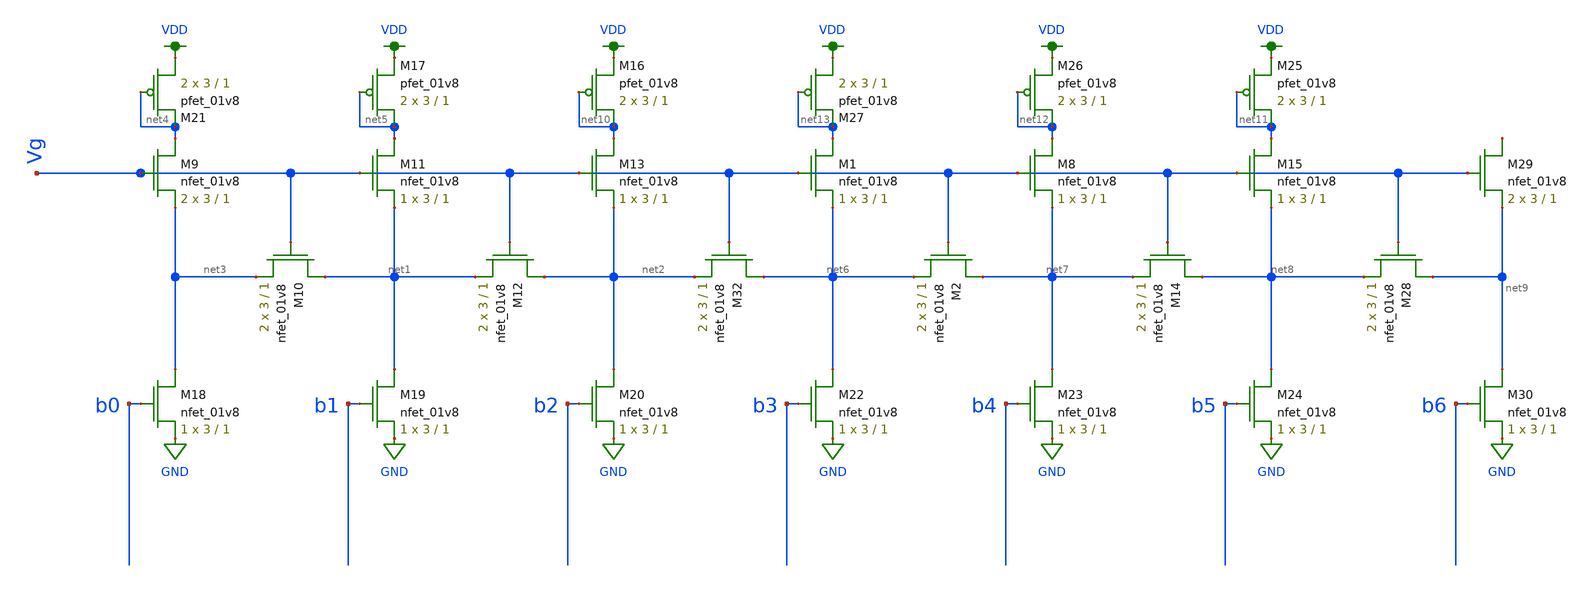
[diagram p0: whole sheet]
** sch_path: schematic/LDS/dac_7_bit.sch
**.subckt dac_7_bit
XM9 net4 Vg net3 GND sky130_fd_pr__nfet_01v8 L=1 W=3 nf=1 ad='int((nf+1)/2) * W/nf * 0.29' as='int((nf+2)/2) * W/nf * 0.29'
+ pd='2*int((nf+1)/2) * (W/nf + 0.29)' ps='2*int((nf+2)/2) * (W/nf + 0.29)' nrd='0.29 / W' nrs='0.29 / W'
+ sa=0 sb=0 sd=0 mult=2 m=2
XM10 net1 Vg net3 GND sky130_fd_pr__nfet_01v8 L=1 W=3 nf=1 ad='int((nf+1)/2) * W/nf * 0.29' as='int((nf+2)/2) * W/nf * 0.29'
+ pd='2*int((nf+1)/2) * (W/nf + 0.29)' ps='2*int((nf+2)/2) * (W/nf + 0.29)' nrd='0.29 / W' nrs='0.29 / W'
+ sa=0 sb=0 sd=0 mult=2 m=2
XM11 net5 Vg net1 GND sky130_fd_pr__nfet_01v8 L=1 W=3 nf=1 ad='int((nf+1)/2) * W/nf * 0.29' as='int((nf+2)/2) * W/nf * 0.29'
+ pd='2*int((nf+1)/2) * (W/nf + 0.29)' ps='2*int((nf+2)/2) * (W/nf + 0.29)' nrd='0.29 / W' nrs='0.29 / W'
+ sa=0 sb=0 sd=0 mult=1 m=1
XM12 net2 Vg net1 GND sky130_fd_pr__nfet_01v8 L=1 W=3 nf=1 ad='int((nf+1)/2) * W/nf * 0.29' as='int((nf+2)/2) * W/nf * 0.29'
+ pd='2*int((nf+1)/2) * (W/nf + 0.29)' ps='2*int((nf+2)/2) * (W/nf + 0.29)' nrd='0.29 / W' nrs='0.29 / W'
+ sa=0 sb=0 sd=0 mult=2 m=2
XM13 net10 Vg net2 GND sky130_fd_pr__nfet_01v8 L=1 W=3 nf=1 ad='int((nf+1)/2) * W/nf * 0.29' as='int((nf+2)/2) * W/nf * 0.29'
+ pd='2*int((nf+1)/2) * (W/nf + 0.29)' ps='2*int((nf+2)/2) * (W/nf + 0.29)' nrd='0.29 / W' nrs='0.29 / W'
+ sa=0 sb=0 sd=0 mult=1 m=1
XM18 net3 b0 GND GND sky130_fd_pr__nfet_01v8 L=1 W=3 nf=1 ad='int((nf+1)/2) * W/nf * 0.29' as='int((nf+2)/2) * W/nf * 0.29'
+ pd='2*int((nf+1)/2) * (W/nf + 0.29)' ps='2*int((nf+2)/2) * (W/nf + 0.29)' nrd='0.29 / W' nrs='0.29 / W'
+ sa=0 sb=0 sd=0 mult=1 m=1
XM19 net1 b1 GND GND sky130_fd_pr__nfet_01v8 L=1 W=3 nf=1 ad='int((nf+1)/2) * W/nf * 0.29' as='int((nf+2)/2) * W/nf * 0.29'
+ pd='2*int((nf+1)/2) * (W/nf + 0.29)' ps='2*int((nf+2)/2) * (W/nf + 0.29)' nrd='0.29 / W' nrs='0.29 / W'
+ sa=0 sb=0 sd=0 mult=1 m=1
XM20 net2 b2 GND GND sky130_fd_pr__nfet_01v8 L=1 W=3 nf=1 ad='int((nf+1)/2) * W/nf * 0.29' as='int((nf+2)/2) * W/nf * 0.29'
+ pd='2*int((nf+1)/2) * (W/nf + 0.29)' ps='2*int((nf+2)/2) * (W/nf + 0.29)' nrd='0.29 / W' nrs='0.29 / W'
+ sa=0 sb=0 sd=0 mult=1 m=1
XM16 net10 net10 VDD VDD sky130_fd_pr__pfet_01v8 L=1 W=3 nf=1 ad='int((nf+1)/2) * W/nf * 0.29' as='int((nf+2)/2) * W/nf * 0.29'
+ pd='2*int((nf+1)/2) * (W/nf + 0.29)' ps='2*int((nf+2)/2) * (W/nf + 0.29)' nrd='0.29 / W' nrs='0.29 / W'
+ sa=0 sb=0 sd=0 mult=2 m=2
XM17 net5 net5 VDD VDD sky130_fd_pr__pfet_01v8 L=1 W=3 nf=1 ad='int((nf+1)/2) * W/nf * 0.29' as='int((nf+2)/2) * W/nf * 0.29'
+ pd='2*int((nf+1)/2) * (W/nf + 0.29)' ps='2*int((nf+2)/2) * (W/nf + 0.29)' nrd='0.29 / W' nrs='0.29 / W'
+ sa=0 sb=0 sd=0 mult=2 m=2
XM21 VDD net4 net4 VDD sky130_fd_pr__pfet_01v8 L=1 W=3 nf=1 ad='int((nf+1)/2) * W/nf * 0.29' as='int((nf+2)/2) * W/nf * 0.29'
+ pd='2*int((nf+1)/2) * (W/nf + 0.29)' ps='2*int((nf+2)/2) * (W/nf + 0.29)' nrd='0.29 / W' nrs='0.29 / W'
+ sa=0 sb=0 sd=0 mult=2 m=2
XM1 net13 Vg net6 GND sky130_fd_pr__nfet_01v8 L=1 W=3 nf=1 ad='int((nf+1)/2) * W/nf * 0.29' as='int((nf+2)/2) * W/nf * 0.29'
+ pd='2*int((nf+1)/2) * (W/nf + 0.29)' ps='2*int((nf+2)/2) * (W/nf + 0.29)' nrd='0.29 / W' nrs='0.29 / W'
+ sa=0 sb=0 sd=0 mult=1 m=1
XM2 net7 Vg net6 GND sky130_fd_pr__nfet_01v8 L=1 W=3 nf=1 ad='int((nf+1)/2) * W/nf * 0.29' as='int((nf+2)/2) * W/nf * 0.29'
+ pd='2*int((nf+1)/2) * (W/nf + 0.29)' ps='2*int((nf+2)/2) * (W/nf + 0.29)' nrd='0.29 / W' nrs='0.29 / W'
+ sa=0 sb=0 sd=0 mult=2 m=2
XM8 net12 Vg net7 GND sky130_fd_pr__nfet_01v8 L=1 W=3 nf=1 ad='int((nf+1)/2) * W/nf * 0.29' as='int((nf+2)/2) * W/nf * 0.29'
+ pd='2*int((nf+1)/2) * (W/nf + 0.29)' ps='2*int((nf+2)/2) * (W/nf + 0.29)' nrd='0.29 / W' nrs='0.29 / W'
+ sa=0 sb=0 sd=0 mult=1 m=1
XM14 net8 Vg net7 GND sky130_fd_pr__nfet_01v8 L=1 W=3 nf=1 ad='int((nf+1)/2) * W/nf * 0.29' as='int((nf+2)/2) * W/nf * 0.29'
+ pd='2*int((nf+1)/2) * (W/nf + 0.29)' ps='2*int((nf+2)/2) * (W/nf + 0.29)' nrd='0.29 / W' nrs='0.29 / W'
+ sa=0 sb=0 sd=0 mult=2 m=2
XM15 net11 Vg net8 GND sky130_fd_pr__nfet_01v8 L=1 W=3 nf=1 ad='int((nf+1)/2) * W/nf * 0.29' as='int((nf+2)/2) * W/nf * 0.29'
+ pd='2*int((nf+1)/2) * (W/nf + 0.29)' ps='2*int((nf+2)/2) * (W/nf + 0.29)' nrd='0.29 / W' nrs='0.29 / W'
+ sa=0 sb=0 sd=0 mult=1 m=1
XM22 net6 b3 GND GND sky130_fd_pr__nfet_01v8 L=1 W=3 nf=1 ad='int((nf+1)/2) * W/nf * 0.29' as='int((nf+2)/2) * W/nf * 0.29'
+ pd='2*int((nf+1)/2) * (W/nf + 0.29)' ps='2*int((nf+2)/2) * (W/nf + 0.29)' nrd='0.29 / W' nrs='0.29 / W'
+ sa=0 sb=0 sd=0 mult=1 m=1
XM23 net7 b4 GND GND sky130_fd_pr__nfet_01v8 L=1 W=3 nf=1 ad='int((nf+1)/2) * W/nf * 0.29' as='int((nf+2)/2) * W/nf * 0.29'
+ pd='2*int((nf+1)/2) * (W/nf + 0.29)' ps='2*int((nf+2)/2) * (W/nf + 0.29)' nrd='0.29 / W' nrs='0.29 / W'
+ sa=0 sb=0 sd=0 mult=1 m=1
XM24 net8 b5 GND GND sky130_fd_pr__nfet_01v8 L=1 W=3 nf=1 ad='int((nf+1)/2) * W/nf * 0.29' as='int((nf+2)/2) * W/nf * 0.29'
+ pd='2*int((nf+1)/2) * (W/nf + 0.29)' ps='2*int((nf+2)/2) * (W/nf + 0.29)' nrd='0.29 / W' nrs='0.29 / W'
+ sa=0 sb=0 sd=0 mult=1 m=1
XM25 net11 net11 VDD VDD sky130_fd_pr__pfet_01v8 L=1 W=3 nf=1 ad='int((nf+1)/2) * W/nf * 0.29' as='int((nf+2)/2) * W/nf * 0.29'
+ pd='2*int((nf+1)/2) * (W/nf + 0.29)' ps='2*int((nf+2)/2) * (W/nf + 0.29)' nrd='0.29 / W' nrs='0.29 / W'
+ sa=0 sb=0 sd=0 mult=2 m=2
XM26 net12 net12 VDD VDD sky130_fd_pr__pfet_01v8 L=1 W=3 nf=1 ad='int((nf+1)/2) * W/nf * 0.29' as='int((nf+2)/2) * W/nf * 0.29'
+ pd='2*int((nf+1)/2) * (W/nf + 0.29)' ps='2*int((nf+2)/2) * (W/nf + 0.29)' nrd='0.29 / W' nrs='0.29 / W'
+ sa=0 sb=0 sd=0 mult=2 m=2
XM27 VDD net13 net13 VDD sky130_fd_pr__pfet_01v8 L=1 W=3 nf=1 ad='int((nf+1)/2) * W/nf * 0.29' as='int((nf+2)/2) * W/nf * 0.29'
+ pd='2*int((nf+1)/2) * (W/nf + 0.29)' ps='2*int((nf+2)/2) * (W/nf + 0.29)' nrd='0.29 / W' nrs='0.29 / W'
+ sa=0 sb=0 sd=0 mult=2 m=2
XM28 net9 Vg net8 GND sky130_fd_pr__nfet_01v8 L=1 W=3 nf=1 ad='int((nf+1)/2) * W/nf * 0.29' as='int((nf+2)/2) * W/nf * 0.29'
+ pd='2*int((nf+1)/2) * (W/nf + 0.29)' ps='2*int((nf+2)/2) * (W/nf + 0.29)' nrd='0.29 / W' nrs='0.29 / W'
+ sa=0 sb=0 sd=0 mult=2 m=2
XM29 net14 Vg net9 GND sky130_fd_pr__nfet_01v8 L=1 W=3 nf=1 ad='int((nf+1)/2) * W/nf * 0.29' as='int((nf+2)/2) * W/nf * 0.29'
+ pd='2*int((nf+1)/2) * (W/nf + 0.29)' ps='2*int((nf+2)/2) * (W/nf + 0.29)' nrd='0.29 / W' nrs='0.29 / W'
+ sa=0 sb=0 sd=0 mult=2 m=2
XM30 net9 b6 GND GND sky130_fd_pr__nfet_01v8 L=1 W=3 nf=1 ad='int((nf+1)/2) * W/nf * 0.29' as='int((nf+2)/2) * W/nf * 0.29'
+ pd='2*int((nf+1)/2) * (W/nf + 0.29)' ps='2*int((nf+2)/2) * (W/nf + 0.29)' nrd='0.29 / W' nrs='0.29 / W'
+ sa=0 sb=0 sd=0 mult=1 m=1
XM32 net6 Vg net2 GND sky130_fd_pr__nfet_01v8 L=1 W=3 nf=1 ad='int((nf+1)/2) * W/nf * 0.29' as='int((nf+2)/2) * W/nf * 0.29'
+ pd='2*int((nf+1)/2) * (W/nf + 0.29)' ps='2*int((nf+2)/2) * (W/nf + 0.29)' nrd='0.29 / W' nrs='0.29 / W'
+ sa=0 sb=0 sd=0 mult=2 m=2
**.ends
.GLOBAL GND
.GLOBAL VDD
.end
